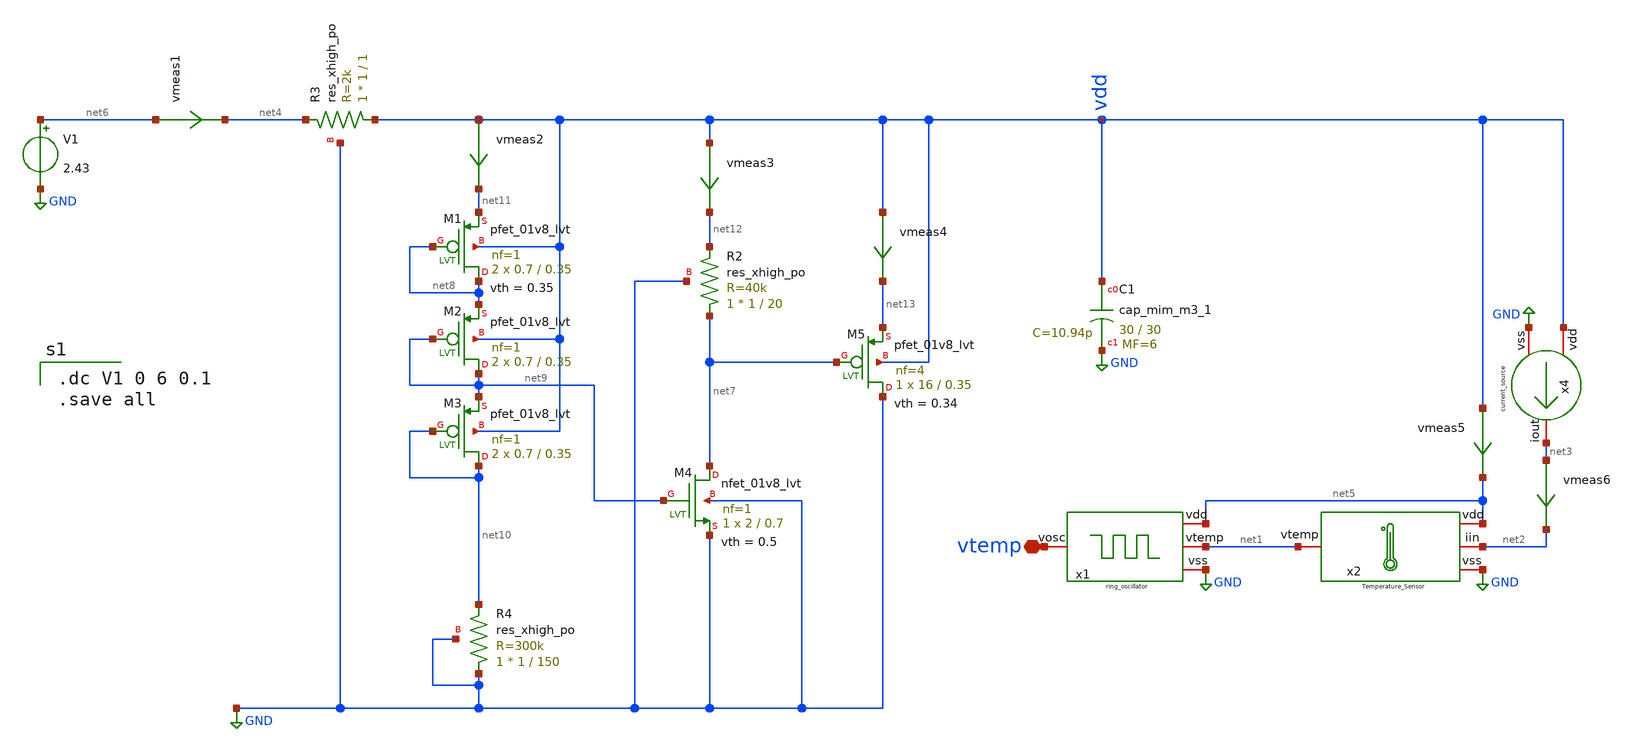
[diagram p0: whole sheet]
** sch_path: XSCHEM/prueba_vlim_2.sch
**.subckt prueba_vlim_2 vtemp
*.iopin vtemp
vmeas6 net3 net2 0
.save i(vmeas6)
vmeas1 net6 net4 0
.save i(vmeas1)
vmeas5 vdd net5 0
.save i(vmeas5)
XC1 vdd GND sky130_fd_pr__cap_mim_m3_1 W=30 L=30 MF=6 m=6
x2 net5 net1 net2 GND Temperature_Sensor
x4 vdd net3 GND current_source
V1 net6 GND 2.43
XM4 net7 net9 GND GND sky130_fd_pr__nfet_01v8_lvt L=0.7 W=2 nf=1 ad='int((nf+1)/2) * W/nf * 0.29' as='int((nf+2)/2) * W/nf * 0.29'
+ pd='2*int((nf+1)/2) * (W/nf + 0.29)' ps='2*int((nf+2)/2) * (W/nf + 0.29)' nrd='0.29 / W' nrs='0.29 / W'
+ sa=0 sb=0 sd=0 mult=1 m=1
XM5 GND net7 net13 vdd sky130_fd_pr__pfet_01v8_lvt L=0.35 W=16 nf=4 ad='int((nf+1)/2) * W/nf * 0.29'
+ as='int((nf+2)/2) * W/nf * 0.29' pd='2*int((nf+1)/2) * (W/nf + 0.29)' ps='2*int((nf+2)/2) * (W/nf + 0.29)'
+ nrd='0.29 / W' nrs='0.29 / W' sa=0 sb=0 sd=0 mult=1 m=1
XM1 net8 net8 net11 vdd sky130_fd_pr__pfet_01v8_lvt L=0.35 W=0.7 nf=1 ad='int((nf+1)/2) * W/nf * 0.29'
+ as='int((nf+2)/2) * W/nf * 0.29' pd='2*int((nf+1)/2) * (W/nf + 0.29)' ps='2*int((nf+2)/2) * (W/nf + 0.29)'
+ nrd='0.29 / W' nrs='0.29 / W' sa=0 sb=0 sd=0 mult=2 m=2
XM2 net9 net9 net8 vdd sky130_fd_pr__pfet_01v8_lvt L=0.35 W=0.7 nf=1 ad='int((nf+1)/2) * W/nf * 0.29'
+ as='int((nf+2)/2) * W/nf * 0.29' pd='2*int((nf+1)/2) * (W/nf + 0.29)' ps='2*int((nf+2)/2) * (W/nf + 0.29)'
+ nrd='0.29 / W' nrs='0.29 / W' sa=0 sb=0 sd=0 mult=2 m=2
XM3 net10 net10 net9 vdd sky130_fd_pr__pfet_01v8_lvt L=0.35 W=0.7 nf=1 ad='int((nf+1)/2) * W/nf * 0.29'
+ as='int((nf+2)/2) * W/nf * 0.29' pd='2*int((nf+1)/2) * (W/nf + 0.29)' ps='2*int((nf+2)/2) * (W/nf + 0.29)'
+ nrd='0.29 / W' nrs='0.29 / W' sa=0 sb=0 sd=0 mult=2 m=2
XR3 vdd net4 GND sky130_fd_pr__res_xhigh_po W=1 L=1 mult=1 m=1
XR2 net7 net12 GND sky130_fd_pr__res_xhigh_po W=1 L=20 mult=1 m=1
XR4 GND net10 GND sky130_fd_pr__res_xhigh_po W=1 L=150 mult=1 m=1
x1 net5 vtemp GND net1 ring_oscillator
vmeas2 vdd net11 0
.save i(vmeas2)
vmeas3 vdd net12 0
.save i(vmeas3)
vmeas4 vdd net13 0
.save i(vmeas4)
**** begin user architecture code

.dc V1 0 6 0.1
.save all


** opencircuitdesign pdks install
.lib $::SKYWATER_MODELS/sky130.lib.spice tt


**** end user architecture code
**.ends
.GLOBAL GND
.end
